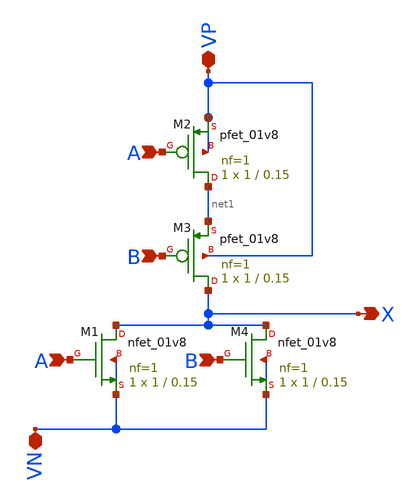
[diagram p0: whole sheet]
** sch_path: projekat_spice/layout/nor/NOR.sch
**.subckt NOR A A B B VP VN X
*.ipin A
*.ipin A
*.ipin B
*.ipin B
*.iopin VP
*.iopin VN
*.opin X
XM1 X A VN VN sky130_fd_pr__nfet_01v8 L=0.15 W=1 nf=1 ad='int((nf+1)/2) * W/nf * 0.29' as='int((nf+2)/2) * W/nf * 0.29'
+ pd='2*int((nf+1)/2) * (W/nf + 0.29)' ps='2*int((nf+2)/2) * (W/nf + 0.29)' nrd='0.29 / W' nrs='0.29 / W'
+ sa=0 sb=0 sd=0 mult=1 m=1
XM2 net1 A VP VP sky130_fd_pr__pfet_01v8 L=0.15 W=1 nf=1 ad='int((nf+1)/2) * W/nf * 0.29' as='int((nf+2)/2) * W/nf * 0.29'
+ pd='2*int((nf+1)/2) * (W/nf + 0.29)' ps='2*int((nf+2)/2) * (W/nf + 0.29)' nrd='0.29 / W' nrs='0.29 / W'
+ sa=0 sb=0 sd=0 mult=1 m=1
XM3 X B net1 VP sky130_fd_pr__pfet_01v8 L=0.15 W=1 nf=1 ad='int((nf+1)/2) * W/nf * 0.29' as='int((nf+2)/2) * W/nf * 0.29'
+ pd='2*int((nf+1)/2) * (W/nf + 0.29)' ps='2*int((nf+2)/2) * (W/nf + 0.29)' nrd='0.29 / W' nrs='0.29 / W'
+ sa=0 sb=0 sd=0 mult=1 m=1
XM4 X B VN VN sky130_fd_pr__nfet_01v8 L=0.15 W=1 nf=1 ad='int((nf+1)/2) * W/nf * 0.29' as='int((nf+2)/2) * W/nf * 0.29'
+ pd='2*int((nf+1)/2) * (W/nf + 0.29)' ps='2*int((nf+2)/2) * (W/nf + 0.29)' nrd='0.29 / W' nrs='0.29 / W'
+ sa=0 sb=0 sd=0 mult=1 m=1
**.ends
.end
